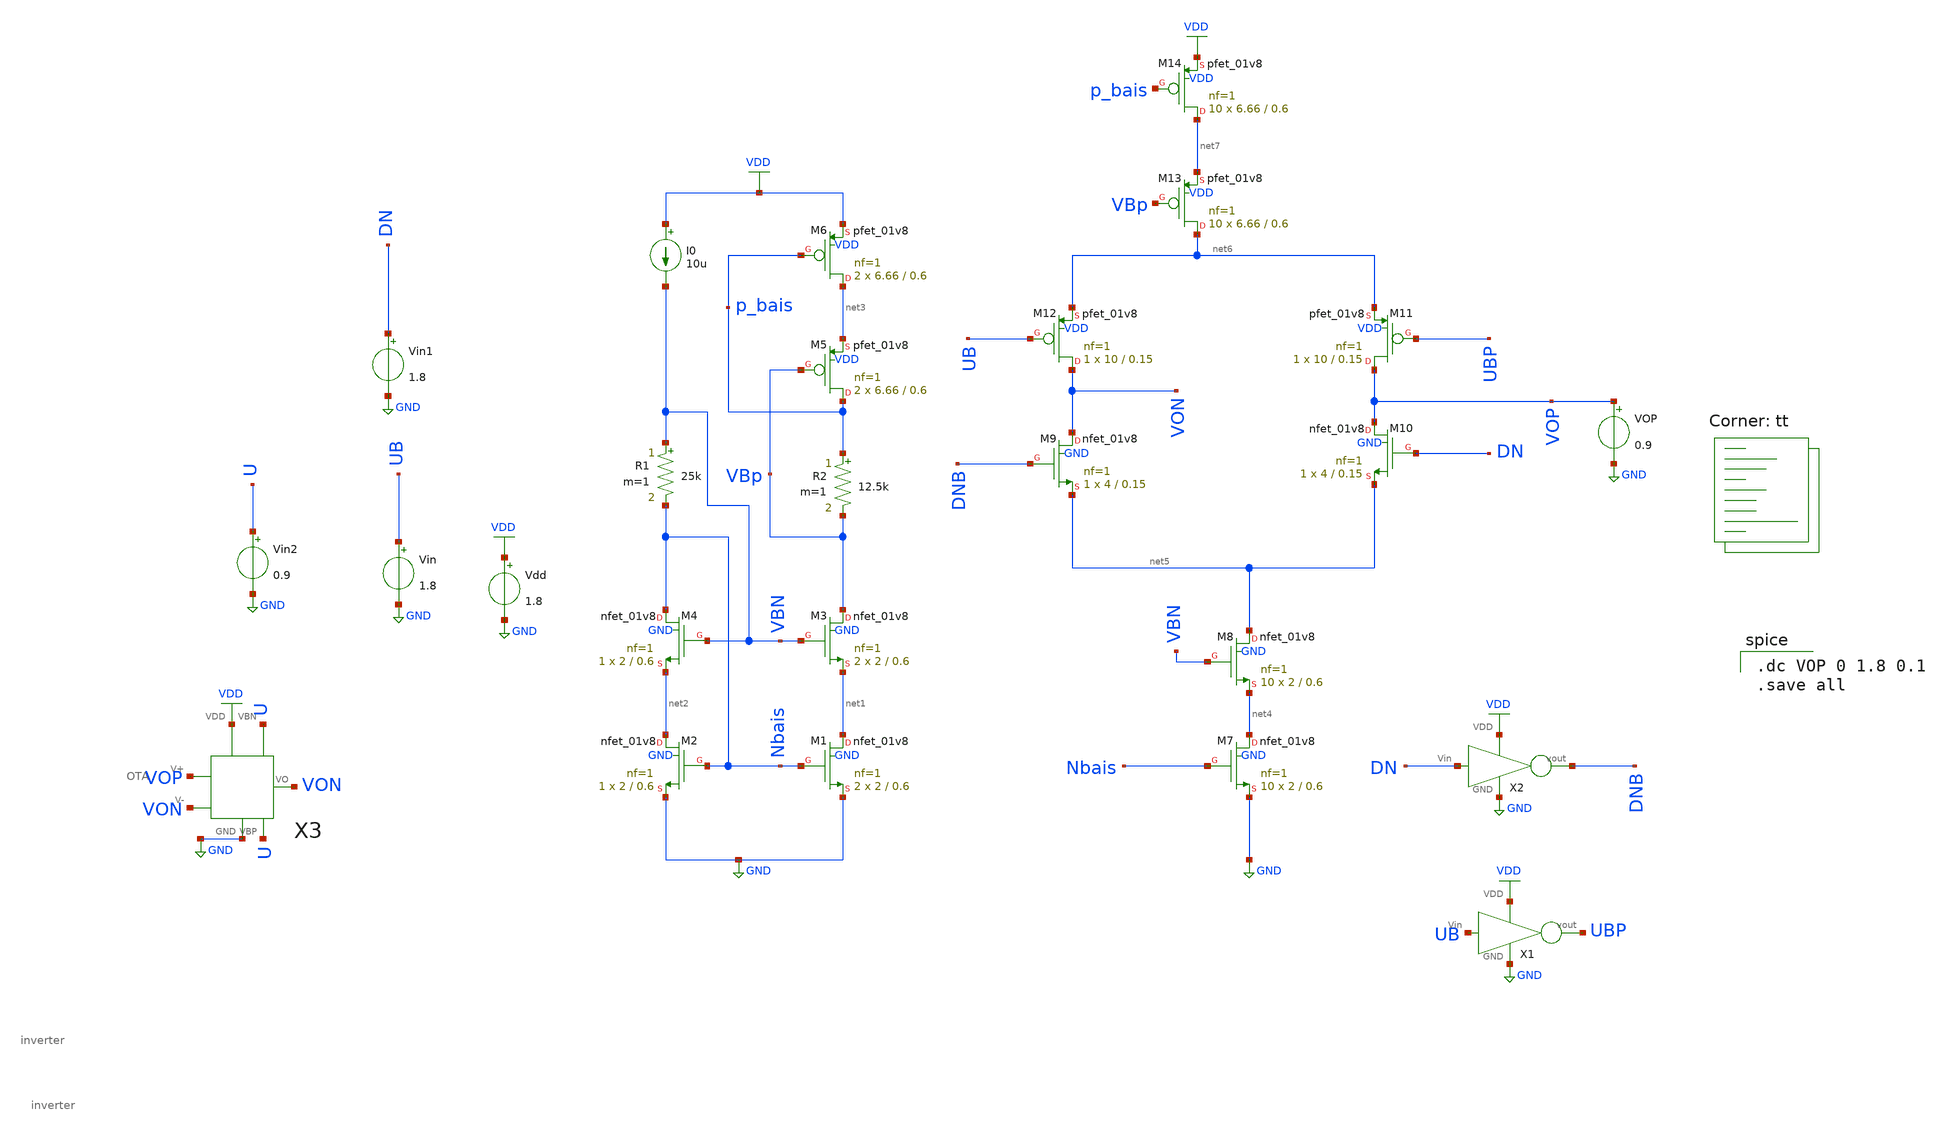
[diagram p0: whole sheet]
** sch_path: pll/pfd_cp_lf_lib/CP/xschem/CP.sch
**.subckt CP
XM1 net1 Nbais GND GND sky130_fd_pr__nfet_01v8 L=0.6 W=2 nf=1 ad='int((nf+1)/2) * W/nf * 0.29' as='int((nf+2)/2) * W/nf * 0.29'
+ pd='2*int((nf+1)/2) * (W/nf + 0.29)' ps='2*int((nf+2)/2) * (W/nf + 0.29)' nrd='0.29 / W' nrs='0.29 / W'
+ sa=0 sb=0 sd=0 mult=2 m=2
XM2 net2 Nbais GND GND sky130_fd_pr__nfet_01v8 L=0.6 W=2 nf=1 ad='int((nf+1)/2) * W/nf * 0.29' as='int((nf+2)/2) * W/nf * 0.29'
+ pd='2*int((nf+1)/2) * (W/nf + 0.29)' ps='2*int((nf+2)/2) * (W/nf + 0.29)' nrd='0.29 / W' nrs='0.29 / W'
+ sa=0 sb=0 sd=0 mult=1 m=1
XM3 VBp VBN net1 GND sky130_fd_pr__nfet_01v8 L=0.6 W=2 nf=1 ad='int((nf+1)/2) * W/nf * 0.29' as='int((nf+2)/2) * W/nf * 0.29'
+ pd='2*int((nf+1)/2) * (W/nf + 0.29)' ps='2*int((nf+2)/2) * (W/nf + 0.29)' nrd='0.29 / W' nrs='0.29 / W'
+ sa=0 sb=0 sd=0 mult=2 m=2
XM4 Nbais VBN net2 GND sky130_fd_pr__nfet_01v8 L=0.6 W=2 nf=1 ad='int((nf+1)/2) * W/nf * 0.29' as='int((nf+2)/2) * W/nf * 0.29'
+ pd='2*int((nf+1)/2) * (W/nf + 0.29)' ps='2*int((nf+2)/2) * (W/nf + 0.29)' nrd='0.29 / W' nrs='0.29 / W'
+ sa=0 sb=0 sd=0 mult=1 m=1
R1 VBN Nbais 25k m=1
R2 p_bais VBp 12.5k m=1
XM5 p_bais VBp net3 VDD sky130_fd_pr__pfet_01v8 L=0.6 W=6.66 nf=1 ad='int((nf+1)/2) * W/nf * 0.29' as='int((nf+2)/2) * W/nf * 0.29'
+ pd='2*int((nf+1)/2) * (W/nf + 0.29)' ps='2*int((nf+2)/2) * (W/nf + 0.29)' nrd='0.29 / W' nrs='0.29 / W'
+ sa=0 sb=0 sd=0 mult=2 m=2
XM6 net3 p_bais VDD VDD sky130_fd_pr__pfet_01v8 L=0.6 W=6.66 nf=1 ad='int((nf+1)/2) * W/nf * 0.29' as='int((nf+2)/2) * W/nf * 0.29'
+ pd='2*int((nf+1)/2) * (W/nf + 0.29)' ps='2*int((nf+2)/2) * (W/nf + 0.29)' nrd='0.29 / W' nrs='0.29 / W'
+ sa=0 sb=0 sd=0 mult=2 m=2
I0 VDD VBN 10u
XM7 net4 Nbais GND GND sky130_fd_pr__nfet_01v8 L=0.6 W=2 nf=1 ad='int((nf+1)/2) * W/nf * 0.29' as='int((nf+2)/2) * W/nf * 0.29'
+ pd='2*int((nf+1)/2) * (W/nf + 0.29)' ps='2*int((nf+2)/2) * (W/nf + 0.29)' nrd='0.29 / W' nrs='0.29 / W'
+ sa=0 sb=0 sd=0 mult=10 m=10
XM8 net5 VBN net4 GND sky130_fd_pr__nfet_01v8 L=0.6 W=2 nf=1 ad='int((nf+1)/2) * W/nf * 0.29' as='int((nf+2)/2) * W/nf * 0.29'
+ pd='2*int((nf+1)/2) * (W/nf + 0.29)' ps='2*int((nf+2)/2) * (W/nf + 0.29)' nrd='0.29 / W' nrs='0.29 / W'
+ sa=0 sb=0 sd=0 mult=10 m=10
XM9 VON DNB net5 GND sky130_fd_pr__nfet_01v8 L=0.15 W=4 nf=1 ad='int((nf+1)/2) * W/nf * 0.29' as='int((nf+2)/2) * W/nf * 0.29'
+ pd='2*int((nf+1)/2) * (W/nf + 0.29)' ps='2*int((nf+2)/2) * (W/nf + 0.29)' nrd='0.29 / W' nrs='0.29 / W'
+ sa=0 sb=0 sd=0 mult=1 m=1
XM10 VOP DN net5 GND sky130_fd_pr__nfet_01v8 L=0.15 W=4 nf=1 ad='int((nf+1)/2) * W/nf * 0.29' as='int((nf+2)/2) * W/nf * 0.29'
+ pd='2*int((nf+1)/2) * (W/nf + 0.29)' ps='2*int((nf+2)/2) * (W/nf + 0.29)' nrd='0.29 / W' nrs='0.29 / W'
+ sa=0 sb=0 sd=0 mult=1 m=1
XM11 VOP UBP net6 VDD sky130_fd_pr__pfet_01v8 L=0.15 W=10 nf=1 ad='int((nf+1)/2) * W/nf * 0.29' as='int((nf+2)/2) * W/nf * 0.29'
+ pd='2*int((nf+1)/2) * (W/nf + 0.29)' ps='2*int((nf+2)/2) * (W/nf + 0.29)' nrd='0.29 / W' nrs='0.29 / W'
+ sa=0 sb=0 sd=0 mult=1 m=1
XM12 VON UB net6 VDD sky130_fd_pr__pfet_01v8 L=0.15 W=10 nf=1 ad='int((nf+1)/2) * W/nf * 0.29' as='int((nf+2)/2) * W/nf * 0.29'
+ pd='2*int((nf+1)/2) * (W/nf + 0.29)' ps='2*int((nf+2)/2) * (W/nf + 0.29)' nrd='0.29 / W' nrs='0.29 / W'
+ sa=0 sb=0 sd=0 mult=1 m=1
XM13 net6 VBp net7 VDD sky130_fd_pr__pfet_01v8 L=0.6 W=6.66 nf=1 ad='int((nf+1)/2) * W/nf * 0.29' as='int((nf+2)/2) * W/nf * 0.29'
+ pd='2*int((nf+1)/2) * (W/nf + 0.29)' ps='2*int((nf+2)/2) * (W/nf + 0.29)' nrd='0.29 / W' nrs='0.29 / W'
+ sa=0 sb=0 sd=0 mult=10 m=10
XM14 net7 p_bais VDD VDD sky130_fd_pr__pfet_01v8 L=0.6 W=6.66 nf=1 ad='int((nf+1)/2) * W/nf * 0.29' as='int((nf+2)/2) * W/nf * 0.29'
+ pd='2*int((nf+1)/2) * (W/nf + 0.29)' ps='2*int((nf+2)/2) * (W/nf + 0.29)' nrd='0.29 / W' nrs='0.29 / W'
+ sa=0 sb=0 sd=0 mult=10 m=10
Vdd VDD GND 1.8
Vin UB GND 1.8
Vin1 DN GND 1.8
VOP VOP GND 0.9
X1 UB UBP VDD GND inverter
X2 DN DNB VDD GND inverter
X3 VOP VON VON VDD GND U U OTA
Vin2 U GND 0.9
**** begin user architecture code
.lib $::SKYWATER_MODELS/sky130.lib.spice tt

.dc VOP 0 1.8 0.1
.save all

**** end user architecture code
**.ends
.GLOBAL GND
.GLOBAL VDD
.end
